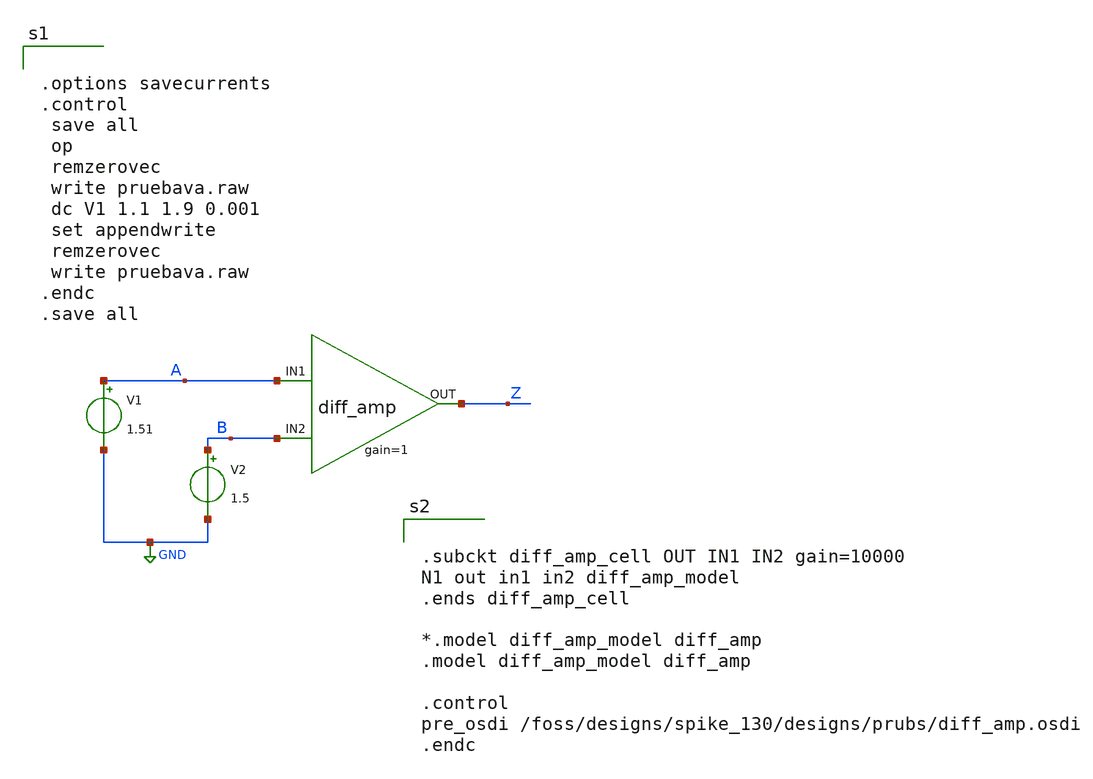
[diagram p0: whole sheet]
** sch_path: designs/prubs/pruebava.sch
**.subckt pruebava
X1 Z A B diff_amp_cell gain=1
V1 A GND 1.51
V2 B GND 1.5
**** begin user architecture code


.options savecurrents
.control
 save all
 op
 remzerovec
 write pruebava.raw
 dc V1 1.1 1.9 0.001
 set appendwrite
 remzerovec
 write pruebava.raw
.endc
.save all




.subckt diff_amp_cell OUT IN1 IN2 gain=10000
N1 out in1 in2 diff_amp_model
.ends diff_amp_cell

*.model diff_amp_model diff_amp
.model diff_amp_model diff_amp

.control
pre_osdi /foss/designs/spike_130/designs/prubs/diff_amp.osdi
.endc

**** end user architecture code
**.ends
.GLOBAL GND
.end
